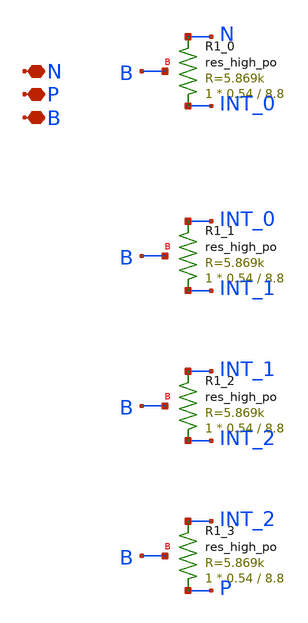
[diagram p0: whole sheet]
** sch_path: ip/sun_tr_sky130nm/design/SUN_TR_SKY130NM/SUNTR_RES25.sch
**.subckt SUNTR_RES25 N P B
*.iopin N
*.iopin P
*.iopin B
XR1_0 INT_0 N B sky130_fd_pr__res_high_po W=0.54 L=8.8 mult=1 m=1
XR1_1 INT_1 INT_0 B sky130_fd_pr__res_high_po W=0.54 L=8.8 mult=1 m=1
XR1_2 INT_2 INT_1 B sky130_fd_pr__res_high_po W=0.54 L=8.8 mult=1 m=1
XR1_3 P INT_2 B sky130_fd_pr__res_high_po W=0.54 L=8.8 mult=1 m=1
**.ends
.end
